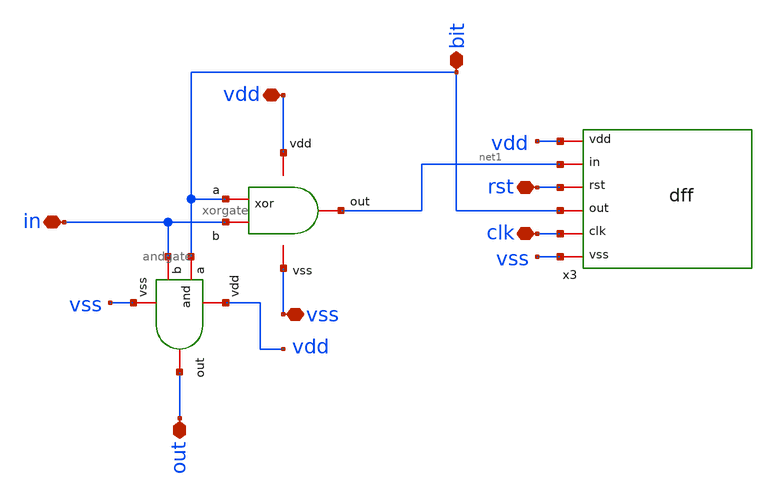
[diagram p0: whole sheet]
** sch_path: design/blocks/count1bit/schematic/count1bit.sch
**.subckt count1bit in clk out rst vss vdd bit
*.iopin in
*.iopin clk
*.iopin out
*.iopin rst
*.iopin vss
*.iopin vdd
*.iopin bit
x2 bit vdd in vss net1 xorgate
x1 vdd bit in out vss andgate
x3 vss clk bit rst net1 vdd dff
**.ends
.end
